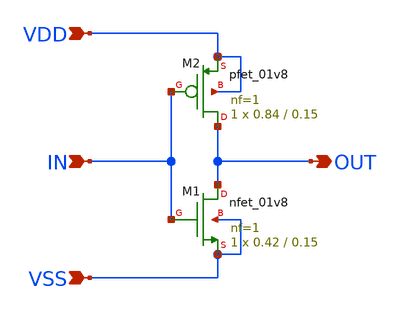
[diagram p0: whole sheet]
** sch_path: hgu/xschem/hgu_inverter.sch
**.subckt hgu_inverter IN VDD VSS OUT
*.ipin IN
*.ipin VDD
*.ipin VSS
*.opin OUT
XM1 OUT IN VSS VSS sky130_fd_pr__nfet_01v8 L=0.15 W=0.42 nf=1 ad='int((nf+1)/2) * W/nf * 0.29' as='int((nf+2)/2) * W/nf * 0.29'
+ pd='2*int((nf+1)/2) * (W/nf + 0.29)' ps='2*int((nf+2)/2) * (W/nf + 0.29)' nrd='0.29 / W' nrs='0.29 / W'
+ sa=0 sb=0 sd=0 mult=1 m=1
XM2 OUT IN VDD VDD sky130_fd_pr__pfet_01v8 L=0.15 W=0.84 nf=1 ad='int((nf+1)/2) * W/nf * 0.29' as='int((nf+2)/2) * W/nf * 0.29'
+ pd='2*int((nf+1)/2) * (W/nf + 0.29)' ps='2*int((nf+2)/2) * (W/nf + 0.29)' nrd='0.29 / W' nrs='0.29 / W'
+ sa=0 sb=0 sd=0 mult=1 m=1
**.ends
.end
